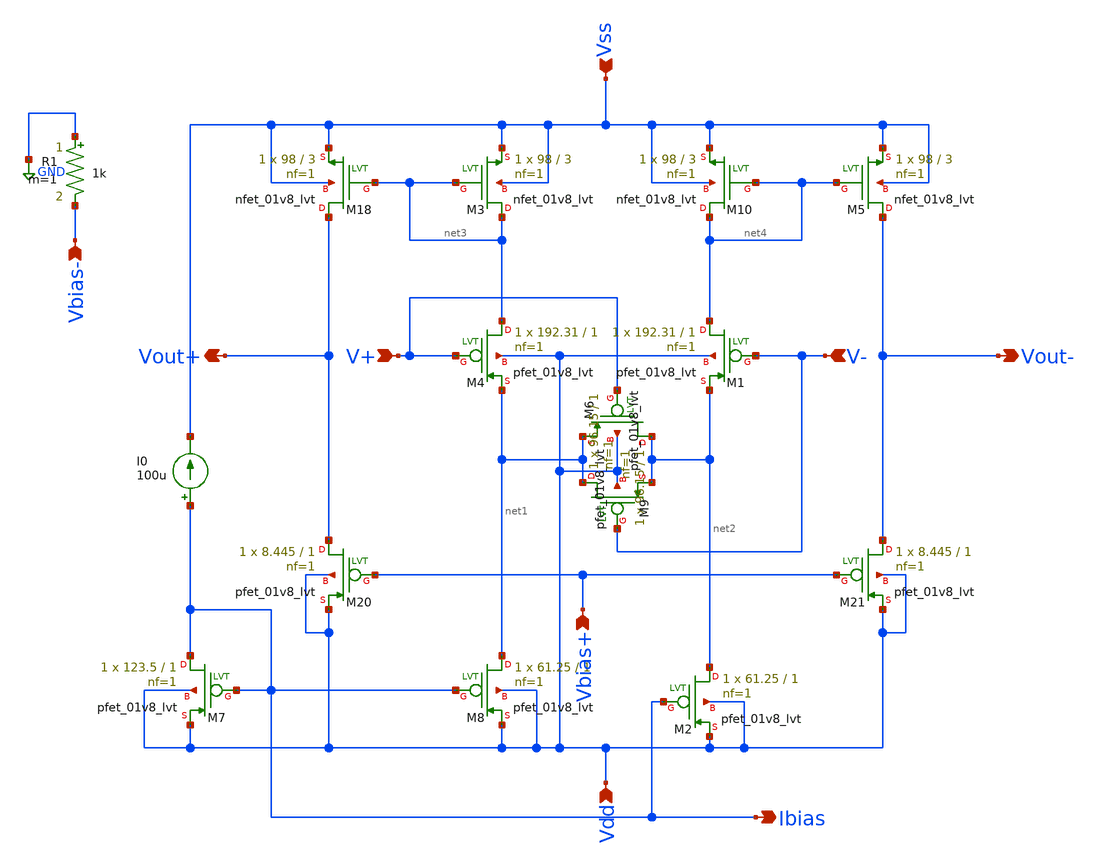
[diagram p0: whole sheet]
** sch_path: xschem/MY_OTA_Full.sch
**.subckt MY_OTA_Full Vout+ Vdd Vss V+ V- Vout- Ibias Vbias- Vbias+
*.opin Vout+
*.ipin Vdd
*.ipin Vss
*.ipin V+
*.ipin V-
*.opin Vout-
*.opin Ibias
*.ipin Vbias-
*.ipin Vbias+
XM7 Ibias Ibias Vdd Vdd sky130_fd_pr__pfet_01v8_lvt L=1 W=123.5 nf=1 ad='int((1 + 1)/2) * 123.5 / 1 * 0.29'
+ as='int((1 + 2)/2) * 123.5 / 1 * 0.29' pd='2*int((1 + 1)/2) * (123.5 / 1 + 0.29)' ps='2*int((1 + 2)/2) * (123.5 / 1 + 0.29)'
+ nrd='0.29 / 123.5 ' nrs='0.29 / 123.5 ' sa=0 sb=0 sd=0 mult=1 m=1
XM8 net1 Ibias Vdd Vdd sky130_fd_pr__pfet_01v8_lvt L=1 W=61.25 nf=1 ad='int((1 + 1)/2) * 61.25 / 1 * 0.29'
+ as='int((1 + 2)/2) * 61.25 / 1 * 0.29' pd='2*int((1 + 1)/2) * (61.25 / 1 + 0.29)' ps='2*int((1 + 2)/2) * (61.25 / 1 + 0.29)'
+ nrd='0.29 / 61.25 ' nrs='0.29 / 61.25 ' sa=0 sb=0 sd=0 mult=1 m=1
XM4 net3 V+ net1 Vdd sky130_fd_pr__pfet_01v8_lvt L=1 W=192.31 nf=1 ad='int((1 + 1)/2) * 192.31 / 1 * 0.29'
+ as='int((1 + 2)/2) * 192.31 / 1 * 0.29' pd='2*int((1 + 1)/2) * (192.31 / 1 + 0.29)' ps='2*int((1 + 2)/2) * (192.31 / 1 + 0.29)'
+ nrd='0.29 / 192.31 ' nrs='0.29 / 192.31 ' sa=0 sb=0 sd=0 mult=1 m=1
XM1 net4 V- net2 Vdd sky130_fd_pr__pfet_01v8_lvt L=1 W=192.31 nf=1 ad='int((1 + 1)/2) * 192.31 / 1 * 0.29'
+ as='int((1 + 2)/2) * 192.31 / 1 * 0.29' pd='2*int((1 + 1)/2) * (192.31 / 1 + 0.29)' ps='2*int((1 + 2)/2) * (192.31 / 1 + 0.29)'
+ nrd='0.29 / 192.31 ' nrs='0.29 / 192.31 ' sa=0 sb=0 sd=0 mult=1 m=1
XM3 net3 net3 Vss Vss sky130_fd_pr__nfet_01v8_lvt L=3 W=98 nf=1 ad='int((1 + 1)/2) * 98 / 1 * 0.29' as='int((1 + 2)/2) * 98 / 1 * 0.29'
+ pd='2*int((1 + 1)/2) * (98 / 1 + 0.29)' ps='2*int((1 + 2)/2) * (98 / 1 + 0.29)' nrd='0.29 / 98 ' nrs='0.29 / 98 '
+ sa=0 sb=0 sd=0 mult=1 m=1
XM2 net2 Ibias Vdd Vdd sky130_fd_pr__pfet_01v8_lvt L=1 W=61.25 nf=1 ad='int((1 + 1)/2) * 61.25 / 1 * 0.29'
+ as='int((1 + 2)/2) * 61.25 / 1 * 0.29' pd='2*int((1 + 1)/2) * (61.25 / 1 + 0.29)' ps='2*int((1 + 2)/2) * (61.25 / 1 + 0.29)'
+ nrd='0.29 / 61.25 ' nrs='0.29 / 61.25 ' sa=0 sb=0 sd=0 mult=1 m=1
XM6 net2 V+ net1 Vdd sky130_fd_pr__pfet_01v8_lvt L=1 W=96.15 nf=1 ad='int((1 + 1)/2) * 96.15 / 1 * 0.29'
+ as='int((1 + 2)/2) * 96.15 / 1 * 0.29' pd='2*int((1 + 1)/2) * (96.15 / 1 + 0.29)' ps='2*int((1 + 2)/2) * (96.15 / 1 + 0.29)'
+ nrd='0.29 / 96.15 ' nrs='0.29 / 96.15 ' sa=0 sb=0 sd=0 mult=1 m=1
XM9 net1 V- net2 Vdd sky130_fd_pr__pfet_01v8_lvt L=1 W=96.15 nf=1 ad='int((1 + 1)/2) * 96.15 / 1 * 0.29'
+ as='int((1 + 2)/2) * 96.15 / 1 * 0.29' pd='2*int((1 + 1)/2) * (96.15 / 1 + 0.29)' ps='2*int((1 + 2)/2) * (96.15 / 1 + 0.29)'
+ nrd='0.29 / 96.15 ' nrs='0.29 / 96.15 ' sa=0 sb=0 sd=0 mult=1 m=1
XM18 Vout+ net3 Vss Vss sky130_fd_pr__nfet_01v8_lvt L=3 W=98 nf=1 ad='int((1 + 1)/2) * 98 / 1 * 0.29'
+ as='int((1 + 2)/2) * 98 / 1 * 0.29' pd='2*int((1 + 1)/2) * (98 / 1 + 0.29)' ps='2*int((1 + 2)/2) * (98 / 1 + 0.29)'
+ nrd='0.29 / 98 ' nrs='0.29 / 98 ' sa=0 sb=0 sd=0 mult=1 m=1
XM5 Vout- net4 Vss Vss sky130_fd_pr__nfet_01v8_lvt L=3 W=98 nf=1 ad='int((1 + 1)/2) * 98 / 1 * 0.29'
+ as='int((1 + 2)/2) * 98 / 1 * 0.29' pd='2*int((1 + 1)/2) * (98 / 1 + 0.29)' ps='2*int((1 + 2)/2) * (98 / 1 + 0.29)'
+ nrd='0.29 / 98 ' nrs='0.29 / 98 ' sa=0 sb=0 sd=0 mult=1 m=1
XM20 Vout+ Vbias+ Vdd Vdd sky130_fd_pr__pfet_01v8_lvt L=1 W=8.445 nf=1 ad='int((1 + 1)/2) * 8.445 / 1 * 0.29'
+ as='int((1 + 2)/2) * 8.445 / 1 * 0.29' pd='2*int((1 + 1)/2) * (8.445 / 1 + 0.29)' ps='2*int((1 + 2)/2) * (8.445 / 1 + 0.29)'
+ nrd='0.29 / 8.445 ' nrs='0.29 / 8.445 ' sa=0 sb=0 sd=0 mult=1 m=1
XM21 Vout- Vbias+ Vdd Vdd sky130_fd_pr__pfet_01v8_lvt L=1 W=8.445 nf=1 ad='int((1 + 1)/2) * 8.445 / 1 * 0.29'
+ as='int((1 + 2)/2) * 8.445 / 1 * 0.29' pd='2*int((1 + 1)/2) * (8.445 / 1 + 0.29)' ps='2*int((1 + 2)/2) * (8.445 / 1 + 0.29)'
+ nrd='0.29 / 8.445 ' nrs='0.29 / 8.445 ' sa=0 sb=0 sd=0 mult=1 m=1
XM10 net4 net4 Vss Vss sky130_fd_pr__nfet_01v8_lvt L=3 W=98 nf=1 ad='int((1 + 1)/2) * 98 / 1 * 0.29'
+ as='int((1 + 2)/2) * 98 / 1 * 0.29' pd='2*int((1 + 1)/2) * (98 / 1 + 0.29)' ps='2*int((1 + 2)/2) * (98 / 1 + 0.29)'
+ nrd='0.29 / 98 ' nrs='0.29 / 98 ' sa=0 sb=0 sd=0 mult=1 m=1
I0 Ibias Vss 100u
R1 GND Vbias- 1k m=1
**.ends
.GLOBAL GND
.end
